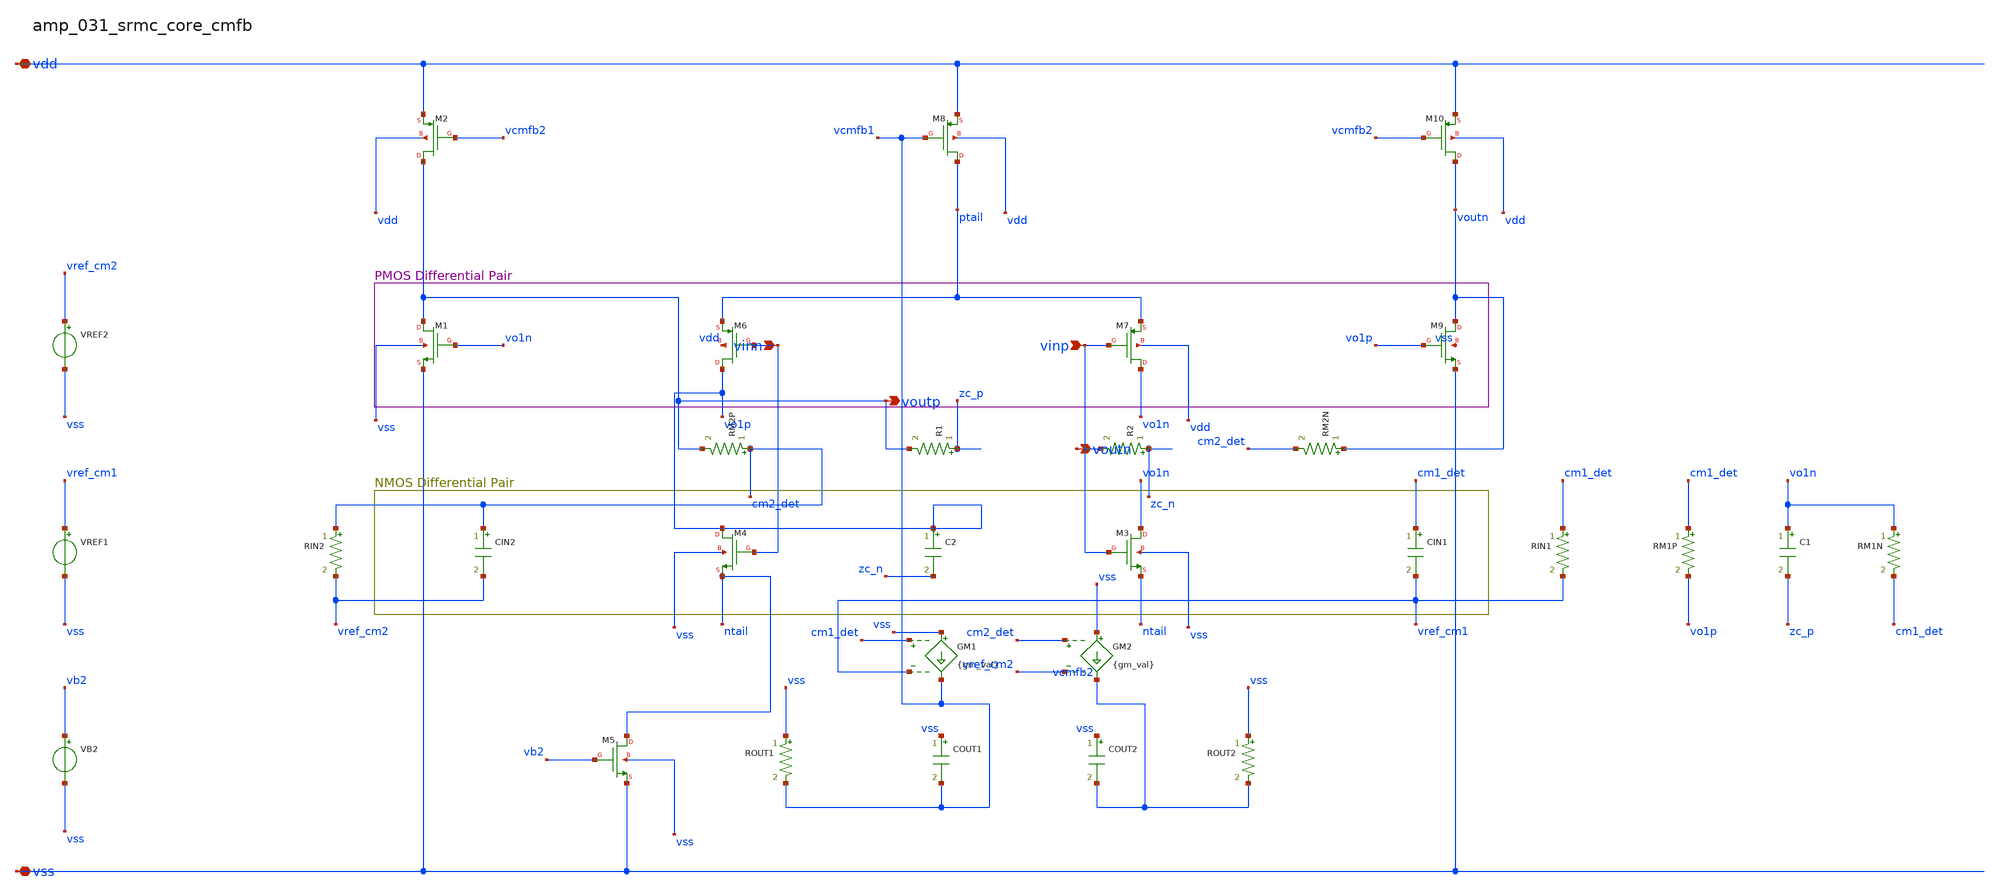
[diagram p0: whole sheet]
** sch_path: analog-db/raw/amp_031_srmc_core_cmfb/amp_031_srmc_core_cmfb_annotated.sch
**.subckt amp_031_srmc_core_cmfb_annotated vinn vinp vdd vss voutp voutn
*.ipin vinn
*.ipin vinp
*.iopin vdd
*.iopin vss
*.opin voutp
*.opin voutn
C1 vo1n zc_p 'x_dut_c1_value' m=1
C2 vo1p zc_n 'x_dut_c2_value' m=1
CIN1 cm1_det vref_cm1 'cin_val' m=1
CIN2 cm2_det vref_cm2 'cin_val' m=1
COUT1 vss vcmfb1 'cout_val' m=1
COUT2 vss vcmfb2 'cout_val' m=1
GM1 vss vcmfb1 cm1_det vref_cm1 {gm_val}
GM2 vss vcmfb2 cm2_det vref_cm2 {gm_val}
R1 zc_p voutp 'x_dut_r1_value' m=1
R2 zc_n voutn 'x_dut_r2_value' m=1
RIN1 cm1_det vref_cm1 'rin_val' m=1
RIN2 cm2_det vref_cm2 'rin_val' m=1
RM1N vo1n cm1_det 'x_dut_rm1n_value' m=1
RM1P cm1_det vo1p 'x_dut_rm1p_value' m=1
RM2N voutn cm2_det 'x_dut_rm2n_value' m=1
RM2P cm2_det voutp 'x_dut_rm2p_value' m=1
ROUT1 vss vcmfb1 'rout_val' m=1
ROUT2 vss vcmfb2 'rout_val' m=1
VB2 vb2 vss dc {vb2}
VREF1 vref_cm1 vss dc {vref_cm}
VREF2 vref_cm2 vss dc {vref_cm}
XM1 voutp vo1n vss vss sg13_lv_nmos w=x_dut_xm1_w l=x_dut_xm1_l ng=1 m=x_dut_xm1_m
XM10 voutn vcmfb2 vdd vdd sg13_lv_pmos w=x_dut_xm10_w l=x_dut_xm10_l ng=1 m=x_dut_xm10_m
XM2 voutp vcmfb2 vdd vdd sg13_lv_pmos w=x_dut_xm2_w l=x_dut_xm2_l ng=1 m=x_dut_xm2_m
XM3 vo1n vinp ntail vss sg13_lv_nmos w=x_dut_xm3_w l=x_dut_xm3_l ng=1 m=x_dut_xm3_m
XM4 vo1p vinn ntail vss sg13_lv_nmos w=x_dut_xm4_w l=x_dut_xm4_l ng=1 m=x_dut_xm4_m
XM5 ntail vb2 vss vss sg13_lv_nmos w=x_dut_xm5_w l=x_dut_xm5_l ng=1 m=x_dut_xm5_m
XM6 vo1p vinn ptail vdd sg13_lv_pmos w=x_dut_xm6_w l=x_dut_xm6_l ng=1 m=x_dut_xm6_m
XM7 vo1n vinp ptail vdd sg13_lv_pmos w=x_dut_xm7_w l=x_dut_xm7_l ng=1 m=x_dut_xm7_m
XM8 ptail vcmfb1 vdd vdd sg13_lv_pmos w=x_dut_xm8_w l=x_dut_xm8_l ng=1 m=x_dut_xm8_m
XM9 voutn vo1p vss vss sg13_lv_nmos w=x_dut_xm9_w l=x_dut_xm9_l ng=1 m=x_dut_xm9_m
**.ends
.end
